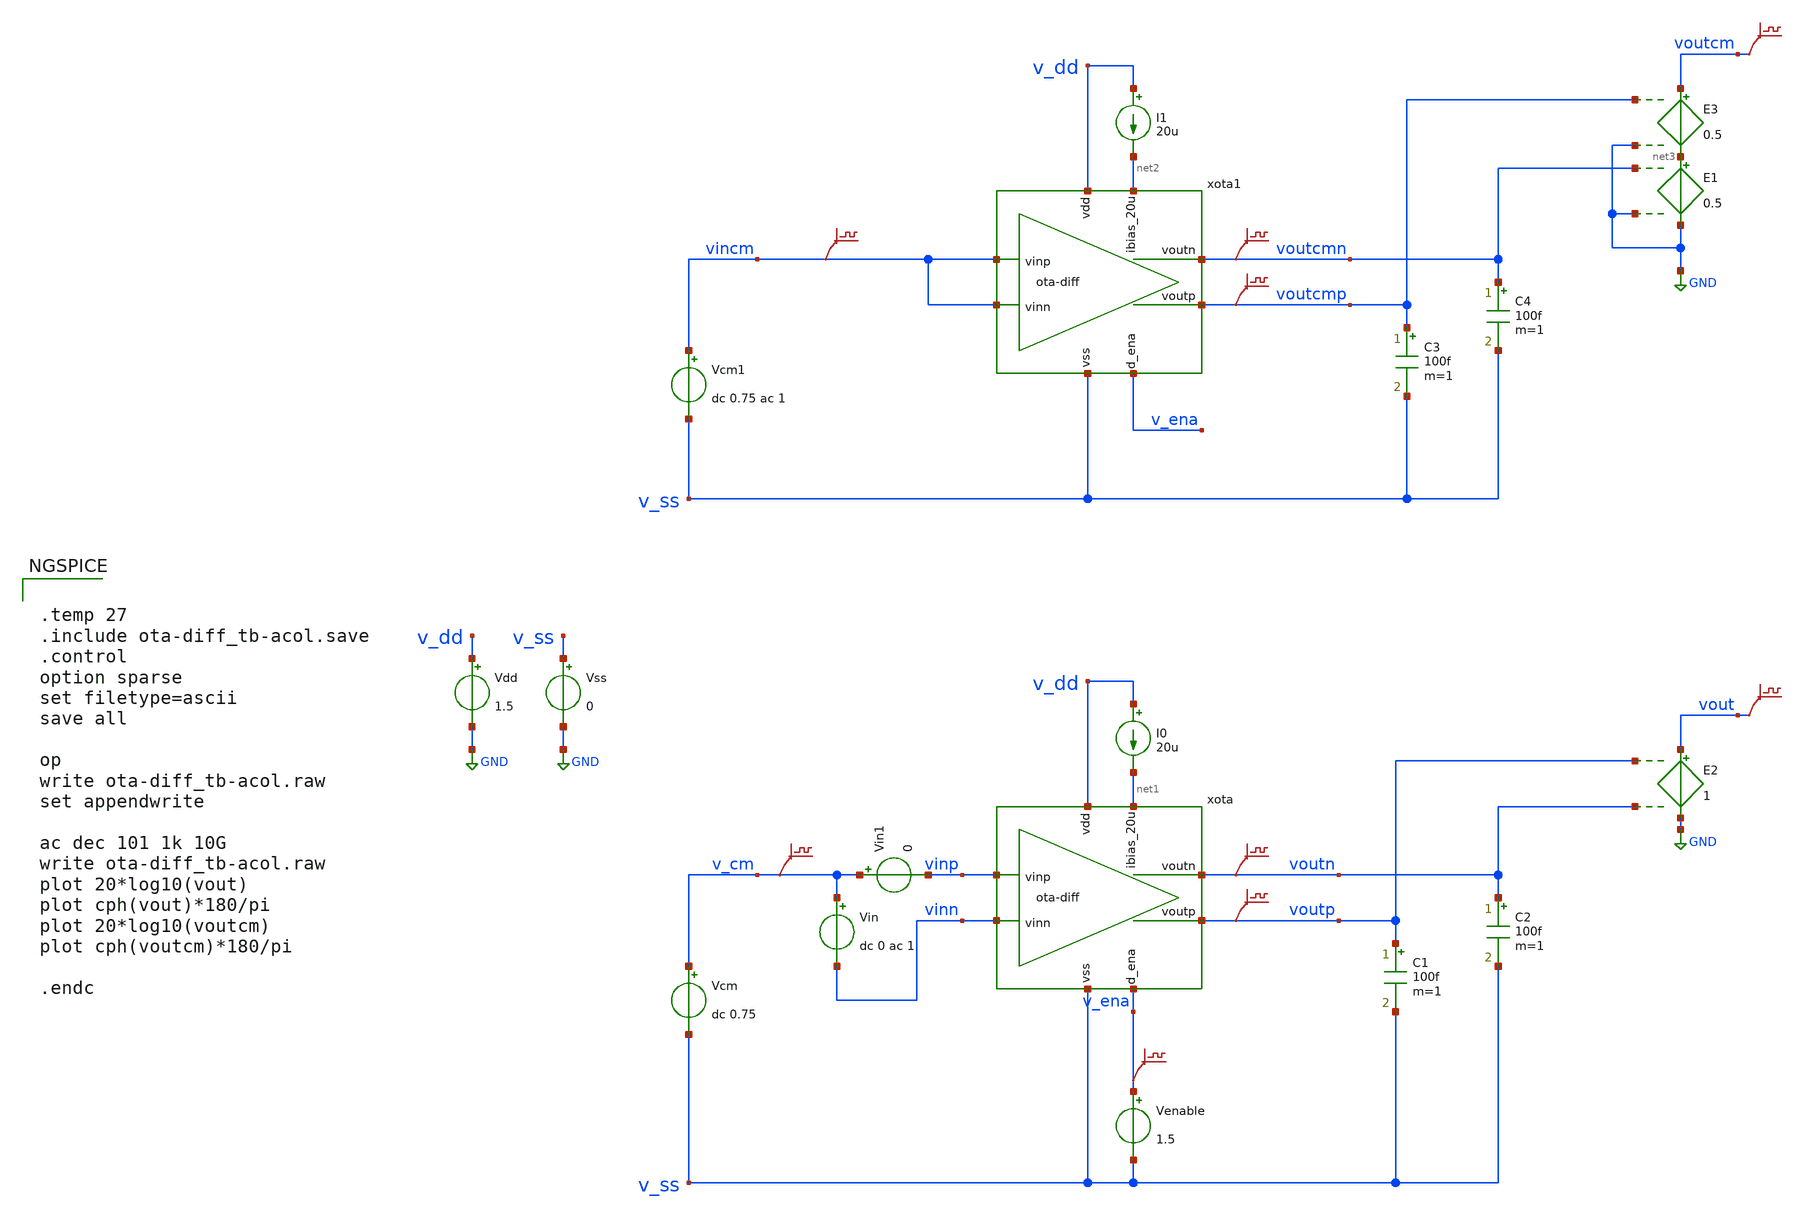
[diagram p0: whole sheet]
** sch_path: xschem/ota-diff_tb-acol.sch
* (c) 2024-2025 Harald Pretl, Apache-2.0 license
* xschem/ota-diff.sch:
* (c) 2025 Harald Pretl, Apache-2.0 license
**.subckt ota-diff_tb-acol
Vdd v_dd GND 1.5
xota v_dd vinp vinn net1 v_ena v_ss voutn voutp ota-diff
Vss v_ss GND 0
C1 voutp v_ss 100f m=1
Vcm v_cm v_ss dc 0.75
I0 v_dd net1 20u
Venable v_ena v_ss 1.5
.save v(v_cm)
.save v(voutp)
.save v(v_ena)
Vin v_cm vinn dc 0 ac 1
C2 voutn v_ss 100f m=1
.save v(voutn)
xota1 v_dd vincm vincm net2 v_ena v_ss voutcmn voutcmp ota-diff
C3 voutcmp v_ss 100f m=1
Vcm1 vincm v_ss dc 0.75 ac 1
I1 v_dd net2 20u
.save v(vincm)
.save v(voutcmp)
C4 voutcmn v_ss 100f m=1
.save v(voutcmn)
E1 net3 GND voutcmn GND 0.5
.save v(voutcm)
E2 vout GND voutp voutn 1
.save v(vout)
E3 voutcm net3 voutcmp GND 0.5
Vin1 v_cm vinp 0
**** begin user architecture code

.lib cornerMOSlv.lib mos_tt
.lib cornerRES.lib res_typ
.lib cornerCAP.lib cap_typ



.temp 27
.include ota-diff_tb-acol.save
.control
option sparse
set filetype=ascii
save all

op
write ota-diff_tb-acol.raw
set appendwrite

ac dec 101 1k 10G
write ota-diff_tb-acol.raw
plot 20*log10(vout)
plot cph(vout)*180/pi
plot 20*log10(voutcm)
plot cph(voutcm)*180/pi

.endc


**** end user architecture code
**.ends

* expanding   symbol:  ota-diff.sym # of pins=8
** sym_path: xschem/ota-diff.sym
** sch_path: xschem/ota-diff.sch
.subckt ota-diff vdd vinp vinn ibias_20u d_ena vss voutn voutp
*.ipin ibias_20u
*.iopin vdd
*.iopin vss
*.ipin vinp
*.ipin vinn
*.opin voutp
*.ipin d_ena
*.opin voutn
XM10 net2 gate_n vss vss sg13_lv_nmos w=200u l=5u ng=40 m=1 mm_ok=1
XM1 vintn vinp tail vss sg13_lv_nmos w=10u l=0.5u ng=2 m=1 mm_ok=1
XM2 vintp vinn tail vss sg13_lv_nmos w=10u l=0.5u ng=2 m=1 mm_ok=1
XM3 vintn gate_p vdd vdd sg13_lv_pmos w=10u l=0.5u ng=2 m=1 mm_ok=1
XM9 ibias_20u gate_n vss vss sg13_lv_nmos w=20u l=5u ng=4 m=1 mm_ok=1
XM16 gate_n ena_n vss vss sg13_lv_nmos w=5u l=0.13u ng=1 m=1 mm_ok=1
XM18 gate_p ena vdd vdd sg13_lv_pmos w=5u l=0.13u ng=1 m=1 mm_ok=1
XM14 ena ena_n vss vss sg13_lv_nmos w=5u l=0.13u ng=1 m=1 mm_ok=1
XM15 ena ena_n vdd vdd sg13_lv_pmos w=5u l=0.13u ng=1 m=1 mm_ok=1
XM17 ibias_20u ena gate_n vss sg13_lv_nmos w=5u l=0.13u ng=1 m=1 mm_ok=1
XM12 ena_n d_ena vss vss sg13_lv_nmos w=5u l=0.13u ng=1 m=1 mm_ok=1
XM13 ena_n d_ena vdd vdd sg13_lv_pmos w=5u l=0.13u ng=1 m=1 mm_ok=1
XM7 voutp net1 vss vss sg13_lv_nmos w=20u l=5u ng=4 m=1 mm_ok=1
XR1 gate_p vintn VSS rhigh w=0.5e-6 l=35e-6 m=1 b=0 mm_ok=1
XR3 net1 voutp VSS rhigh w=0.5e-6 l=60e-6 m=1 b=0 mm_ok=1
XM11_1 net3 gate_n net8 vss sg13_lv_nmos w=5u l=5u ng=1 m=1 mm_ok=1
XM5 vintp gate_p vdd vdd sg13_lv_pmos w=10u l=0.5u ng=2 m=1 mm_ok=1
XM4 net4 vintn vdd vdd sg13_lv_pmos w=10u l=0.5u ng=2 m=1 mm_ok=1
XM6 net5 vintp vdd vdd sg13_lv_pmos w=10u l=0.5u ng=2 m=1 mm_ok=1
XR2 gate_p vintp VSS rhigh w=0.5e-6 l=35e-6 m=1 b=0 mm_ok=1
XM8 voutn net1 vss vss sg13_lv_nmos w=20u l=5u ng=4 m=1 mm_ok=1
XR4 net1 voutn VSS rhigh w=0.5e-6 l=60e-6 m=1 b=0 mm_ok=1
Vmeas tail net2 0
.save i(vmeas)
Vmeas1 net4 voutp 0
.save i(vmeas1)
Vmeas2 net5 voutn 0
.save i(vmeas2)
Vmeas3 net1 net3 0
.save i(vmeas3)
XCstab1 gate_p net7 cap_cmim w=80e-6 l=20e-6 m=1 mm_ok=1
XCstab2 gate_p net6 cap_cmim w=80e-6 l=20e-6 m=1 mm_ok=1
XRstab11 net7 vintn VSS rppd w=0.5e-6 l=5e-6 m=1 b=0 mm_ok=1
XRstab12 net7 vintn VSS rppd w=0.5e-6 l=5e-6 m=1 b=0 mm_ok=1
XRstab13 net7 vintn VSS rppd w=0.5e-6 l=5e-6 m=1 b=0 mm_ok=1
XRstab14 net7 vintn VSS rppd w=0.5e-6 l=5e-6 m=1 b=0 mm_ok=1
XRstab21 net6 vintp VSS rppd w=0.5e-6 l=5e-6 m=1 b=0 mm_ok=1
XRstab22 net6 vintp VSS rppd w=0.5e-6 l=5e-6 m=1 b=0 mm_ok=1
XRstab23 net6 vintp VSS rppd w=0.5e-6 l=5e-6 m=1 b=0 mm_ok=1
XRstab24 net6 vintp VSS rppd w=0.5e-6 l=5e-6 m=1 b=0 mm_ok=1
XM11 net8 gate_n vss vss sg13_lv_nmos w=5u l=5u ng=1 m=1 mm_ok=1
.ends

.GLOBAL GND
.end
